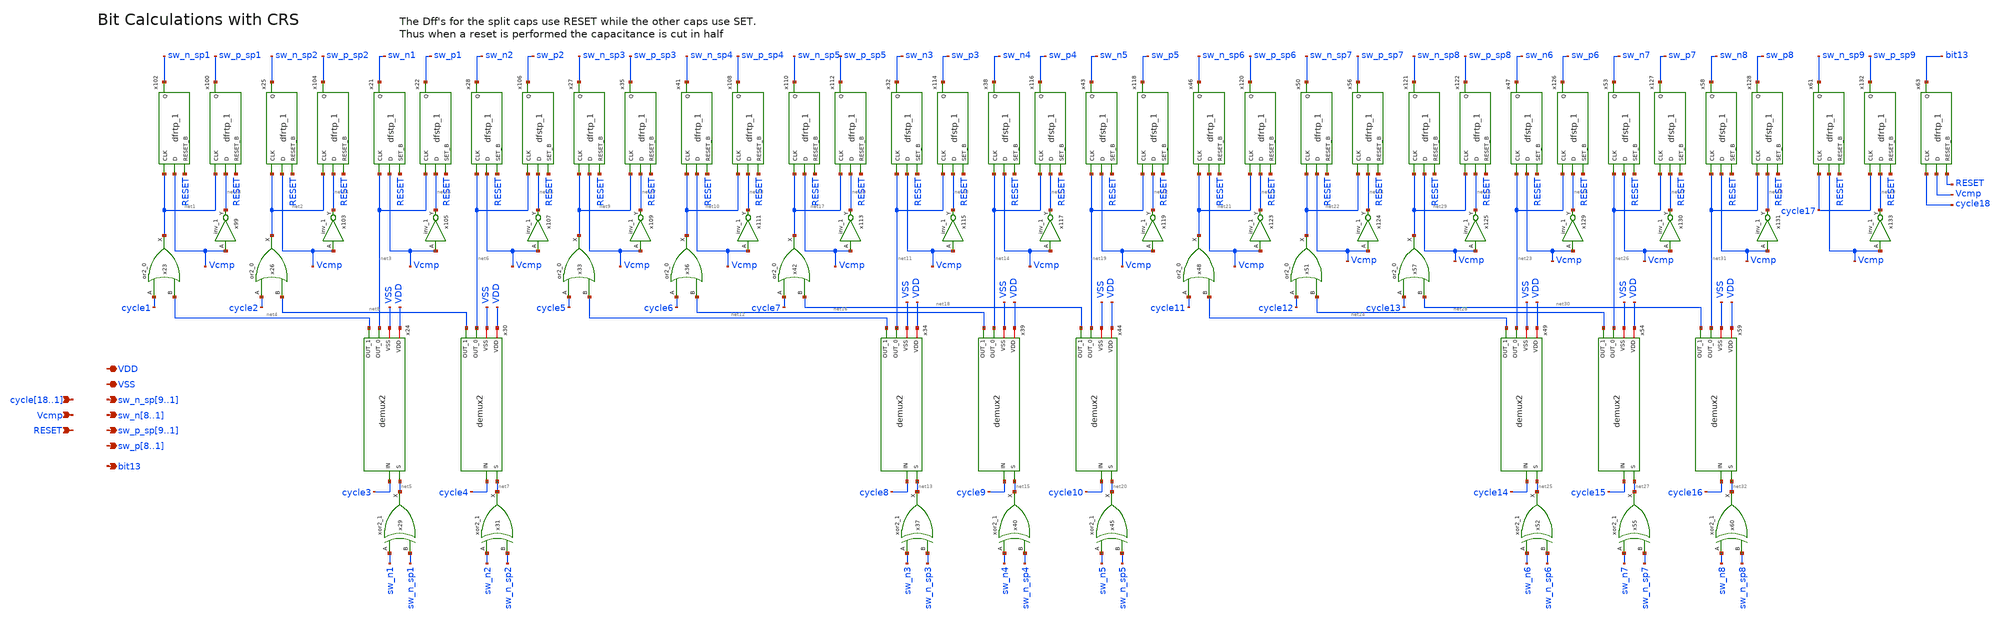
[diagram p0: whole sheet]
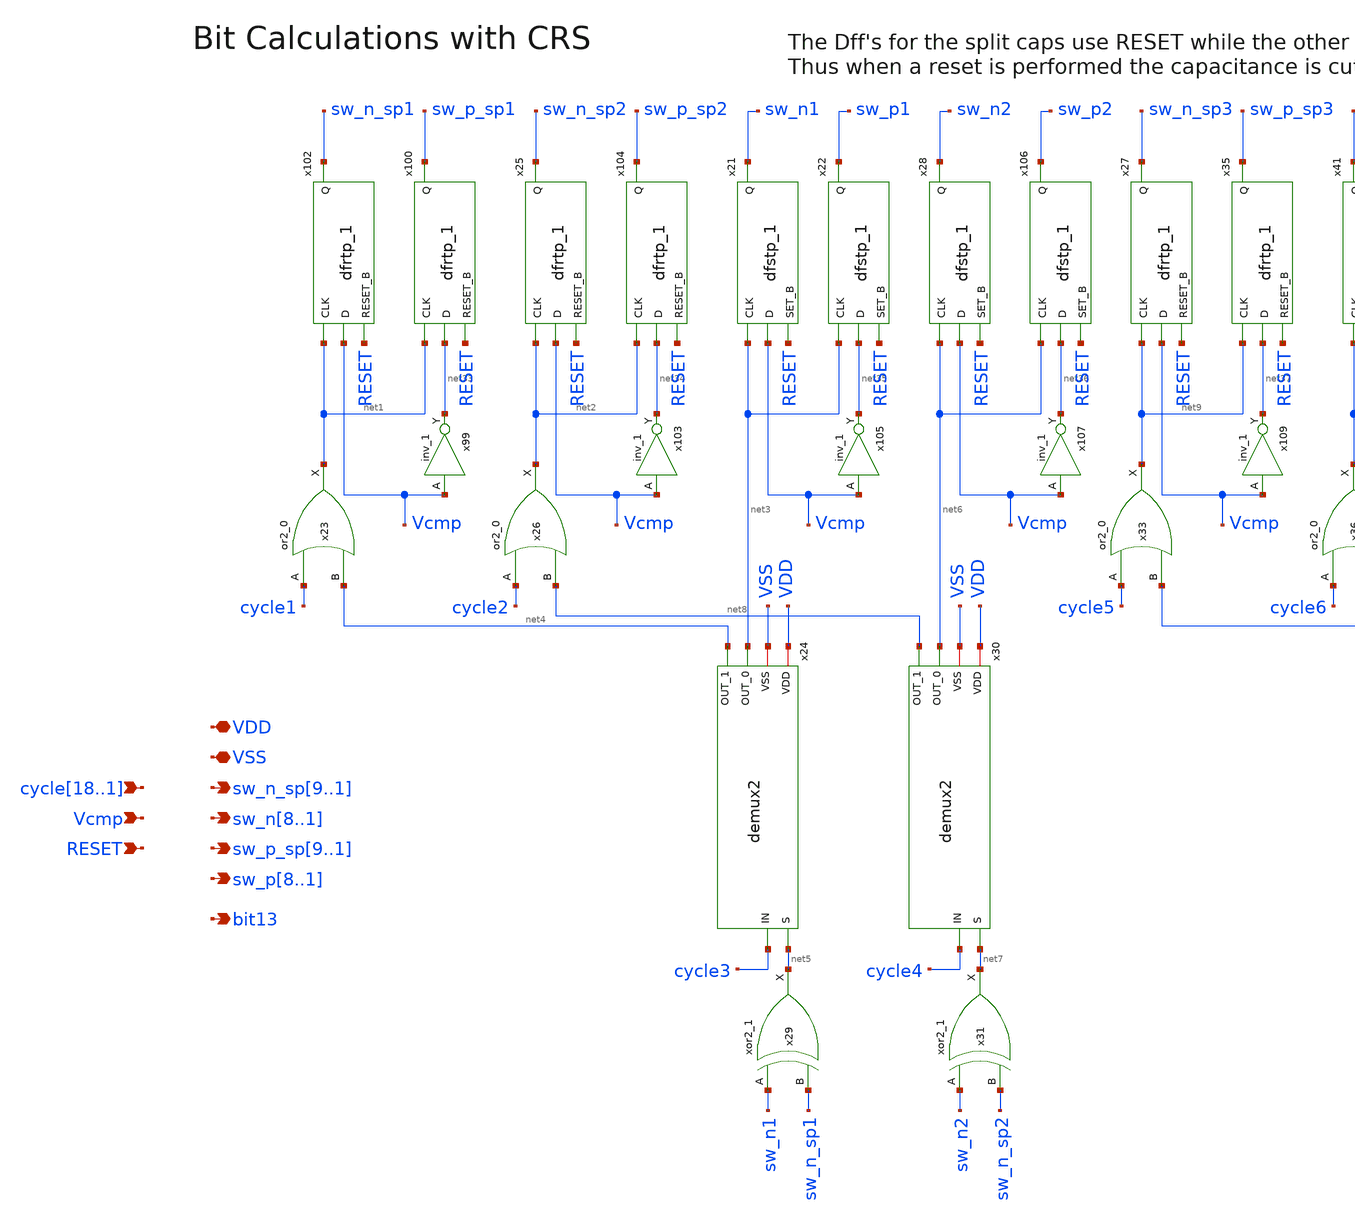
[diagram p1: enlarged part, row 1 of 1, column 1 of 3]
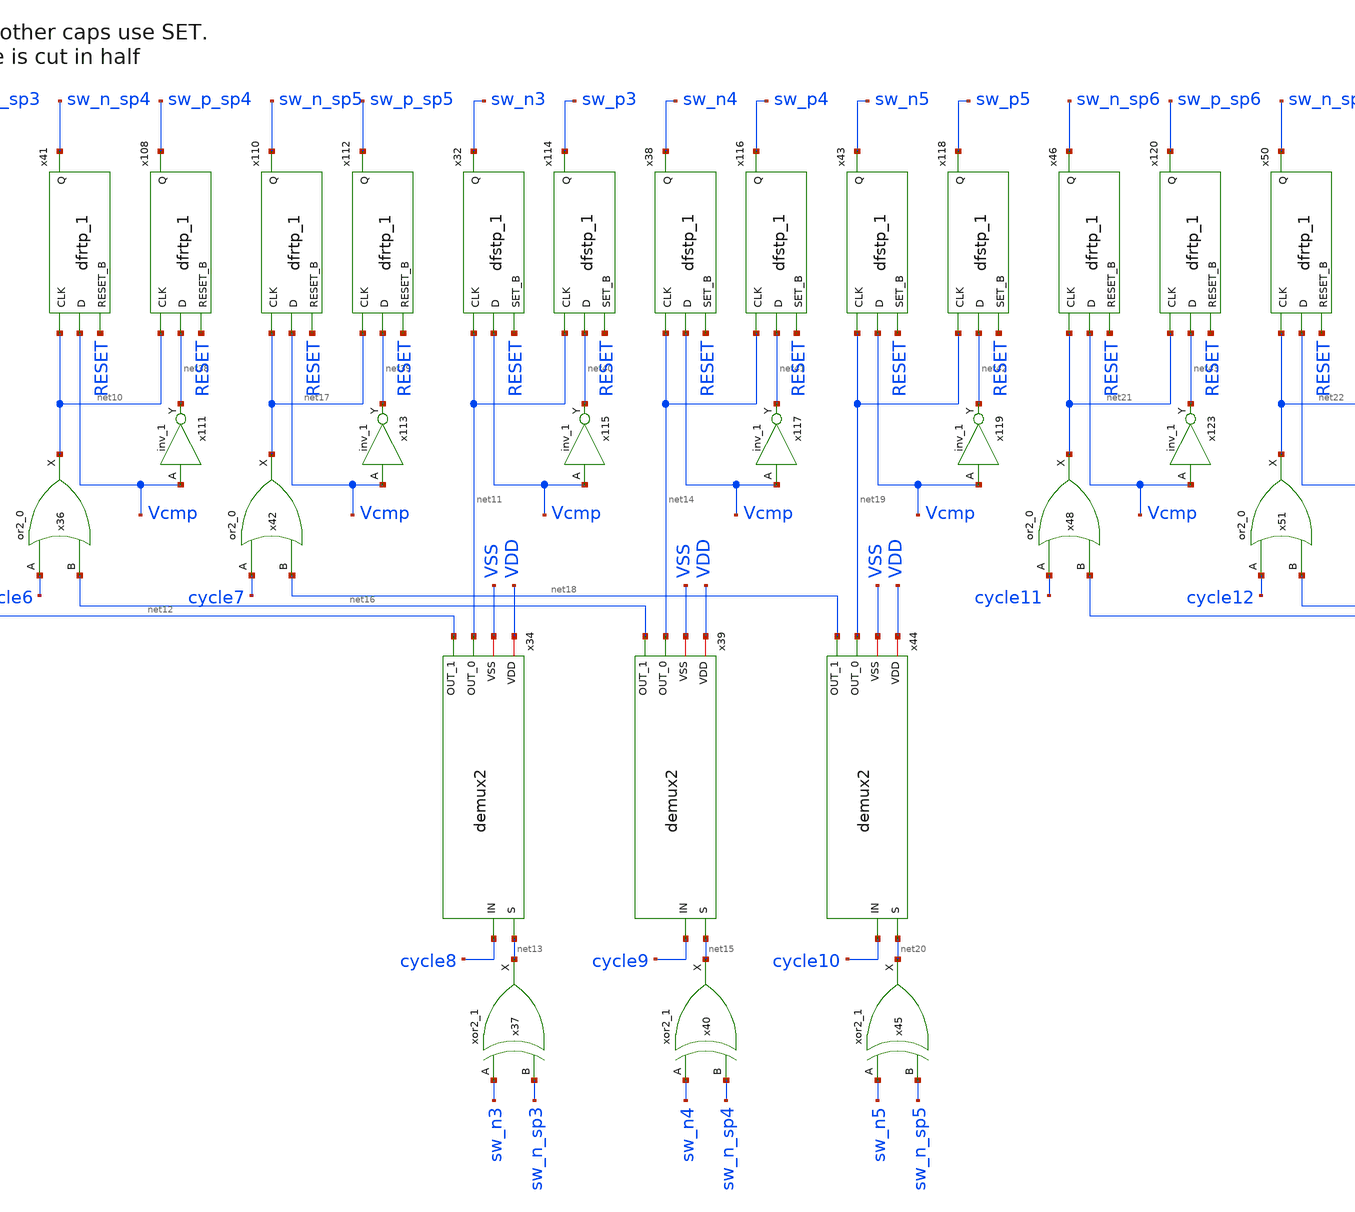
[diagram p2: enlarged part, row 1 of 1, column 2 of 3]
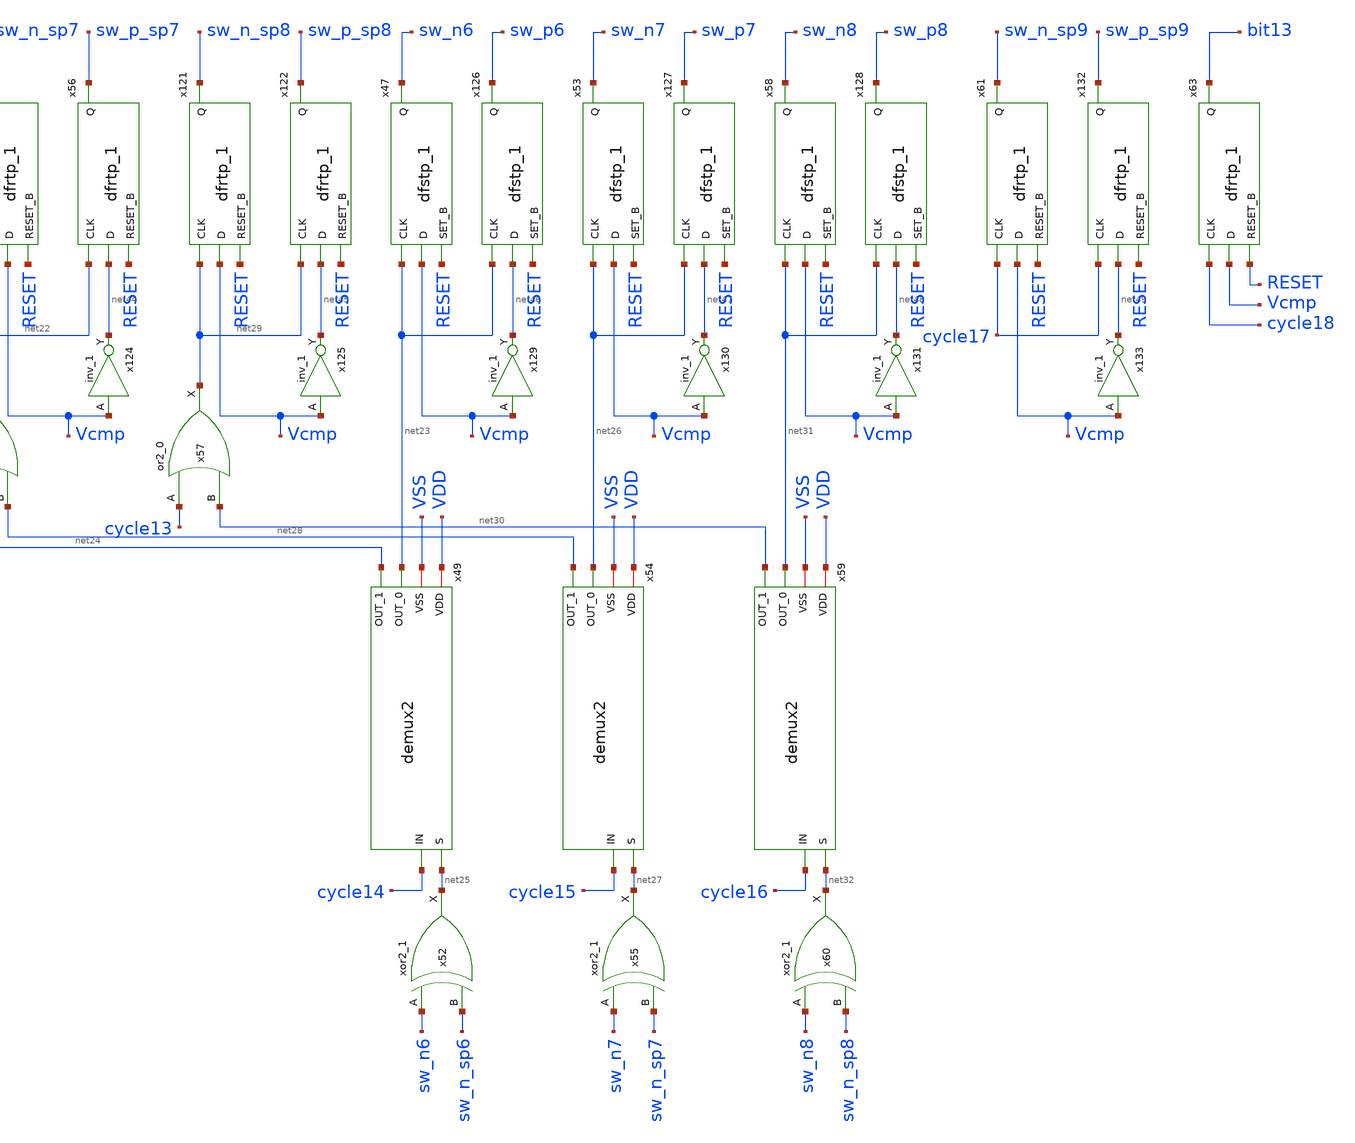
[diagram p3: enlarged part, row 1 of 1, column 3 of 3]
** sch_path: xschem/src/raw_bit_calculator/raw_bit_calculator.sch
**.subckt raw_bit_calculator
*+ cycle18,cycle17,cycle16,cycle15,cycle14,cycle13,cycle12,cycle11,cycle10,cycle9,cycle8,cycle7,cycle6,cycle5,cycle4,cycle3,cycle2,cycle1 sw_n_sp9,sw_n_sp8,sw_n_sp7,sw_n_sp6,sw_n_sp5,sw_n_sp4,sw_n_sp3,sw_n_sp2,sw_n_sp1 VSS VDD
*+ sw_n8,sw_n7,sw_n6,sw_n5,sw_n4,sw_n3,sw_n2,sw_n1 sw_p_sp9,sw_p_sp8,sw_p_sp7,sw_p_sp6,sw_p_sp5,sw_p_sp4,sw_p_sp3,sw_p_sp2,sw_p_sp1
*+ sw_p8,sw_p7,sw_p6,sw_p5,sw_p4,sw_p3,sw_p2,sw_p1 Vcmp RESET bit13
*.ipin
*+ cycle18,cycle17,cycle16,cycle15,cycle14,cycle13,cycle12,cycle11,cycle10,cycle9,cycle8,cycle7,cycle6,cycle5,cycle4,cycle3,cycle2,cycle1
*.opin sw_n_sp9,sw_n_sp8,sw_n_sp7,sw_n_sp6,sw_n_sp5,sw_n_sp4,sw_n_sp3,sw_n_sp2,sw_n_sp1
*.iopin VSS
*.iopin VDD
*.opin sw_n8,sw_n7,sw_n6,sw_n5,sw_n4,sw_n3,sw_n2,sw_n1
*.opin sw_p_sp9,sw_p_sp8,sw_p_sp7,sw_p_sp6,sw_p_sp5,sw_p_sp4,sw_p_sp3,sw_p_sp2,sw_p_sp1
*.opin sw_p8,sw_p7,sw_p6,sw_p5,sw_p4,sw_p3,sw_p2,sw_p1
*.ipin Vcmp
*.ipin RESET
*.opin bit13
x23 cycle1 net4 VSS VSS VDD VDD net1 sky130_fd_sc_hd__or2_0
x26 cycle2 net8 VSS VSS VDD VDD net2 sky130_fd_sc_hd__or2_0
x29 sw_n1 sw_n_sp1 VSS VSS VDD VDD net5 sky130_fd_sc_hd__xor2_1
x31 sw_n2 sw_n_sp2 VSS VSS VDD VDD net7 sky130_fd_sc_hd__xor2_1
x33 cycle5 net12 VSS VSS VDD VDD net9 sky130_fd_sc_hd__or2_0
x36 cycle6 net16 VSS VSS VDD VDD net10 sky130_fd_sc_hd__or2_0
x37 sw_n3 sw_n_sp3 VSS VSS VDD VDD net13 sky130_fd_sc_hd__xor2_1
x40 sw_n4 sw_n_sp4 VSS VSS VDD VDD net15 sky130_fd_sc_hd__xor2_1
x42 cycle7 net18 VSS VSS VDD VDD net17 sky130_fd_sc_hd__or2_0
x45 sw_n5 sw_n_sp5 VSS VSS VDD VDD net20 sky130_fd_sc_hd__xor2_1
x48 cycle11 net24 VSS VSS VDD VDD net21 sky130_fd_sc_hd__or2_0
x51 cycle12 net28 VSS VSS VDD VDD net22 sky130_fd_sc_hd__or2_0
x52 sw_n6 sw_n_sp6 VSS VSS VDD VDD net25 sky130_fd_sc_hd__xor2_1
x55 sw_n7 sw_n_sp7 VSS VSS VDD VDD net27 sky130_fd_sc_hd__xor2_1
x57 cycle13 net30 VSS VSS VDD VDD net29 sky130_fd_sc_hd__or2_0
x60 sw_n8 sw_n_sp8 VSS VSS VDD VDD net32 sky130_fd_sc_hd__xor2_1
x63 cycle18 Vcmp RESET VSS VSS VDD VDD bit13 sky130_fd_sc_hd__dfrtp_1
x100 net1 net33 RESET VSS VSS VDD VDD sw_p_sp1 sky130_fd_sc_hd__dfrtp_1
x99 Vcmp VSS VSS VDD VDD net33 sky130_fd_sc_hd__inv_1
x102 net1 Vcmp RESET VSS VSS VDD VDD sw_n_sp1 sky130_fd_sc_hd__dfrtp_1
x25 net2 Vcmp RESET VSS VSS VDD VDD sw_n_sp2 sky130_fd_sc_hd__dfrtp_1
x103 Vcmp VSS VSS VDD VDD net34 sky130_fd_sc_hd__inv_1
x104 net2 net34 RESET VSS VSS VDD VDD sw_p_sp2 sky130_fd_sc_hd__dfrtp_1
x21 net3 Vcmp RESET VSS VSS VDD VDD sw_n1 sky130_fd_sc_hd__dfstp_1
x22 net3 net35 RESET VSS VSS VDD VDD sw_p1 sky130_fd_sc_hd__dfstp_1
x105 Vcmp VSS VSS VDD VDD net35 sky130_fd_sc_hd__inv_1
x28 net6 Vcmp RESET VSS VSS VDD VDD sw_n2 sky130_fd_sc_hd__dfstp_1
x106 net6 net36 RESET VSS VSS VDD VDD sw_p2 sky130_fd_sc_hd__dfstp_1
x107 Vcmp VSS VSS VDD VDD net36 sky130_fd_sc_hd__inv_1
x109 Vcmp VSS VSS VDD VDD net37 sky130_fd_sc_hd__inv_1
x111 Vcmp VSS VSS VDD VDD net38 sky130_fd_sc_hd__inv_1
x27 net9 Vcmp RESET VSS VSS VDD VDD sw_n_sp3 sky130_fd_sc_hd__dfrtp_1
x35 net9 net37 RESET VSS VSS VDD VDD sw_p_sp3 sky130_fd_sc_hd__dfrtp_1
x41 net10 Vcmp RESET VSS VSS VDD VDD sw_n_sp4 sky130_fd_sc_hd__dfrtp_1
x108 net10 net38 RESET VSS VSS VDD VDD sw_p_sp4 sky130_fd_sc_hd__dfrtp_1
x110 net17 Vcmp RESET VSS VSS VDD VDD sw_n_sp5 sky130_fd_sc_hd__dfrtp_1
x112 net17 net39 RESET VSS VSS VDD VDD sw_p_sp5 sky130_fd_sc_hd__dfrtp_1
x113 Vcmp VSS VSS VDD VDD net39 sky130_fd_sc_hd__inv_1
x114 net11 net40 RESET VSS VSS VDD VDD sw_p3 sky130_fd_sc_hd__dfstp_1
x32 net11 Vcmp RESET VSS VSS VDD VDD sw_n3 sky130_fd_sc_hd__dfstp_1
x115 Vcmp VSS VSS VDD VDD net40 sky130_fd_sc_hd__inv_1
x38 net14 Vcmp RESET VSS VSS VDD VDD sw_n4 sky130_fd_sc_hd__dfstp_1
x116 net14 net41 RESET VSS VSS VDD VDD sw_p4 sky130_fd_sc_hd__dfstp_1
x117 Vcmp VSS VSS VDD VDD net41 sky130_fd_sc_hd__inv_1
x43 net19 Vcmp RESET VSS VSS VDD VDD sw_n5 sky130_fd_sc_hd__dfstp_1
x118 net19 net42 RESET VSS VSS VDD VDD sw_p5 sky130_fd_sc_hd__dfstp_1
x119 Vcmp VSS VSS VDD VDD net42 sky130_fd_sc_hd__inv_1
x120 net21 net43 RESET VSS VSS VDD VDD sw_p_sp6 sky130_fd_sc_hd__dfrtp_1
x46 net21 Vcmp RESET VSS VSS VDD VDD sw_n_sp6 sky130_fd_sc_hd__dfrtp_1
x50 net22 Vcmp RESET VSS VSS VDD VDD sw_n_sp7 sky130_fd_sc_hd__dfrtp_1
x56 net22 net44 RESET VSS VSS VDD VDD sw_p_sp7 sky130_fd_sc_hd__dfrtp_1
x121 net29 Vcmp RESET VSS VSS VDD VDD sw_n_sp8 sky130_fd_sc_hd__dfrtp_1
x122 net29 net45 RESET VSS VSS VDD VDD sw_p_sp8 sky130_fd_sc_hd__dfrtp_1
x123 Vcmp VSS VSS VDD VDD net43 sky130_fd_sc_hd__inv_1
x124 Vcmp VSS VSS VDD VDD net44 sky130_fd_sc_hd__inv_1
x125 Vcmp VSS VSS VDD VDD net45 sky130_fd_sc_hd__inv_1
x126 net23 net46 RESET VSS VSS VDD VDD sw_p6 sky130_fd_sc_hd__dfstp_1
x47 net23 Vcmp RESET VSS VSS VDD VDD sw_n6 sky130_fd_sc_hd__dfstp_1
x53 net26 Vcmp RESET VSS VSS VDD VDD sw_n7 sky130_fd_sc_hd__dfstp_1
x58 net31 Vcmp RESET VSS VSS VDD VDD sw_n8 sky130_fd_sc_hd__dfstp_1
x127 net26 net47 RESET VSS VSS VDD VDD sw_p7 sky130_fd_sc_hd__dfstp_1
x128 net31 net48 RESET VSS VSS VDD VDD sw_p8 sky130_fd_sc_hd__dfstp_1
x129 Vcmp VSS VSS VDD VDD net46 sky130_fd_sc_hd__inv_1
x130 Vcmp VSS VSS VDD VDD net47 sky130_fd_sc_hd__inv_1
x131 Vcmp VSS VSS VDD VDD net48 sky130_fd_sc_hd__inv_1
x132 cycle17 net49 RESET VSS VSS VDD VDD sw_p_sp9 sky130_fd_sc_hd__dfrtp_1
x133 Vcmp VSS VSS VDD VDD net49 sky130_fd_sc_hd__inv_1
x61 cycle17 Vcmp RESET VSS VSS VDD VDD sw_n_sp9 sky130_fd_sc_hd__dfrtp_1
x24 net5 VDD VSS net3 cycle3 net4 demux2
x30 net7 VDD VSS net6 cycle4 net8 demux2
x34 net13 VDD VSS net11 cycle8 net12 demux2
x39 net15 VDD VSS net14 cycle9 net16 demux2
x44 net20 VDD VSS net19 cycle10 net18 demux2
x49 net25 VDD VSS net23 cycle14 net24 demux2
x54 net27 VDD VSS net26 cycle15 net28 demux2
x59 net32 VDD VSS net31 cycle16 net30 demux2
**.ends

* expanding   symbol:  src/demux2/demux2.sym # of pins=6
** sym_path: xschem/src/demux2/demux2.sym
** sch_path: xschem/src/demux2/demux2.sch
.subckt demux2 S VDD VSS OUT_0 IN OUT_1
*.ipin S
*.opin OUT_0
*.ipin IN
*.opin OUT_1
*.iopin VDD
*.iopin VSS
x1 net1 IN VSS VSS VDD VDD OUT_0 sky130_fd_sc_hd__and2_0
x2 S IN VSS VSS VDD VDD OUT_1 sky130_fd_sc_hd__and2_0
x3 S VSS VSS VDD VDD net1 sky130_fd_sc_hd__inv_1
.ends

.end
